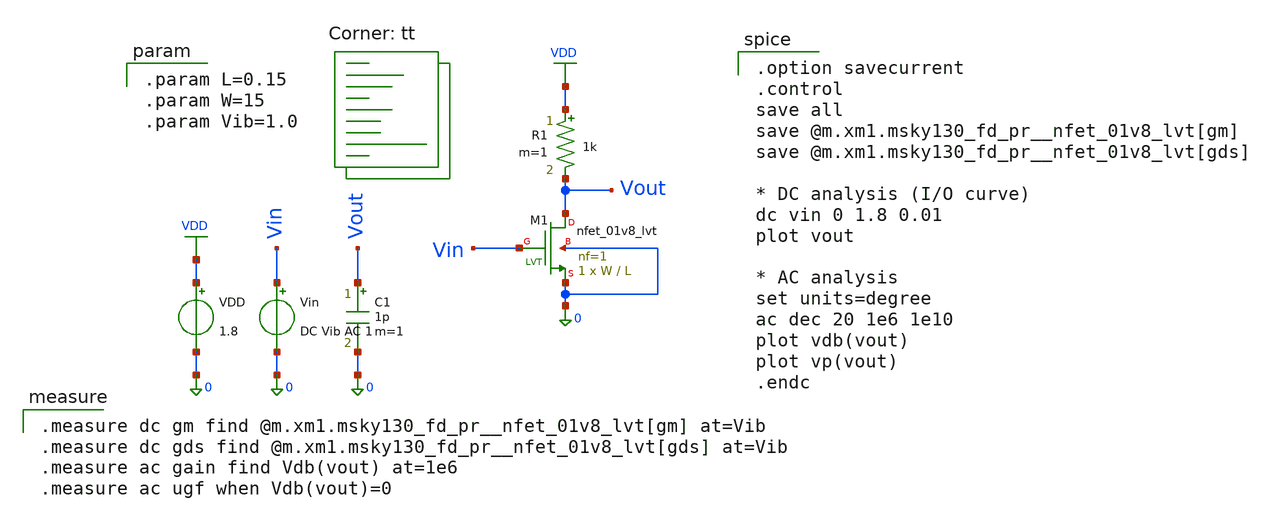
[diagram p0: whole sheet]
** sch_path: cs.sch
**.subckt cs
XM1 Vout Vin 0 0 sky130_fd_pr__nfet_01v8_lvt L=L W=W nf=1 ad='int((1 + 1)/2) * W / 1 * 0.29' as='int((1 + 2)/2) * W / 1 * 0.29'
+ pd='2*int((1 + 1)/2) * (W / 1 + 0.29)' ps='2*int((1 + 2)/2) * (W / 1 + 0.29)' nrd='0.29 / W ' nrs='0.29 / W '
+ sa=0 sb=0 sd=0 mult=1 m=1
R1 VDD Vout 1k m=1
VDD VDD 0 1.8
Vin Vin 0 DC Vib AC 1
C1 Vout 0 1p m=1
**** begin user architecture code

.param L=0.15
.param W=15
.param Vib=1.0


.measure dc gm find @m.xm1.msky130_fd_pr__nfet_01v8_lvt[gm] at=Vib
.measure dc gds find @m.xm1.msky130_fd_pr__nfet_01v8_lvt[gds] at=Vib
.measure ac gain find Vdb(vout) at=1e6
.measure ac ugf when Vdb(vout)=0


.option savecurrent
.control
save all
save @m.xm1.msky130_fd_pr__nfet_01v8_lvt[gm]
save @m.xm1.msky130_fd_pr__nfet_01v8_lvt[gds]

* DC analysis (I/O curve)
dc vin 0 1.8 0.01
plot vout

* AC analysis
set units=degree
ac dec 20 1e6 1e10
plot vdb(vout)
plot vp(vout)
.endc

.lib $::SKYWATER_MODELS/sky130.lib.spice tt
**** end user architecture code
**.ends
.GLOBAL VDD
.end
